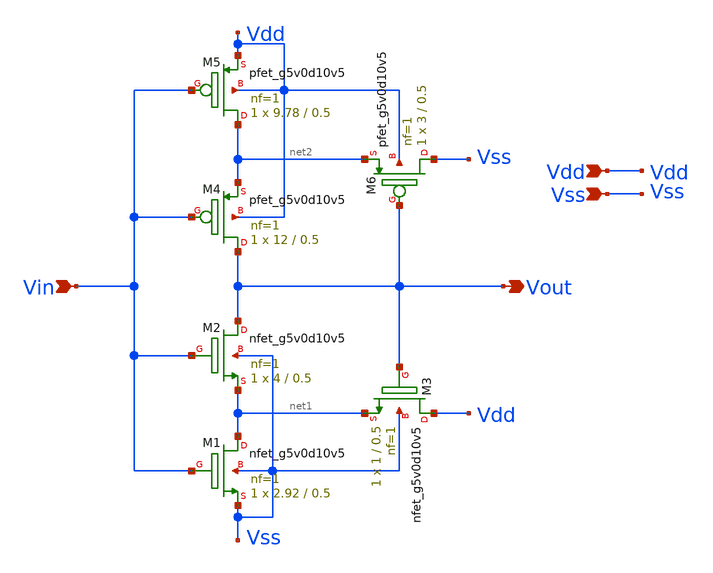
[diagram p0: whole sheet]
** sch_path: xschem/Schmitt.sch
**.subckt Schmitt Vout Vin Vdd Vss
*.opin Vout
*.ipin Vin
*.ipin Vdd
*.ipin Vss
XM1 net1 Vin Vss Vss sky130_fd_pr__nfet_g5v0d10v5 L=0.5 W=2.92 nf=1 ad='int((1 + 1)/2) * 2.92 / 1 * 0.29'
+ as='int((1 + 2)/2) * 2.92 / 1 * 0.29' pd='2*int((1 + 1)/2) * (2.92 / 1 + 0.29)' ps='2*int((1 + 2)/2) * (2.92 / 1 + 0.29)'
+ nrd='0.29 / 2.92 ' nrs='0.29 / 2.92 ' sa=0 sb=0 sd=0 mult=1 m=1
XM5 net2 Vin Vdd Vdd sky130_fd_pr__pfet_g5v0d10v5 L=0.5 W=9.78 nf=1 ad='int((1 + 1)/2) * 9.78 / 1 * 0.29'
+ as='int((1 + 2)/2) * 9.78 / 1 * 0.29' pd='2*int((1 + 1)/2) * (9.78 / 1 + 0.29)' ps='2*int((1 + 2)/2) * (9.78 / 1 + 0.29)'
+ nrd='0.29 / 9.78 ' nrs='0.29 / 9.78 ' sa=0 sb=0 sd=0 mult=1 m=1
XM3 Vdd Vout net1 Vss sky130_fd_pr__nfet_g5v0d10v5 L=0.5 W=1 nf=1 ad='int((1 + 1)/2) * 1 / 1 * 0.29'
+ as='int((1 + 2)/2) * 1 / 1 * 0.29' pd='2*int((1 + 1)/2) * (1 / 1 + 0.29)' ps='2*int((1 + 2)/2) * (1 / 1 + 0.29)'
+ nrd='0.29 / 1 ' nrs='0.29 / 1 ' sa=0 sb=0 sd=0 mult=1 m=1
XM2 Vout Vin net1 Vss sky130_fd_pr__nfet_g5v0d10v5 L=0.5 W=4 nf=1 ad='int((1 + 1)/2) * 4 / 1 * 0.29'
+ as='int((1 + 2)/2) * 4 / 1 * 0.29' pd='2*int((1 + 1)/2) * (4 / 1 + 0.29)' ps='2*int((1 + 2)/2) * (4 / 1 + 0.29)'
+ nrd='0.29 / 4 ' nrs='0.29 / 4 ' sa=0 sb=0 sd=0 mult=1 m=1
XM6 Vss Vout net2 Vdd sky130_fd_pr__pfet_g5v0d10v5 L=0.5 W=3 nf=1 ad='int((1 + 1)/2) * 3 / 1 * 0.29'
+ as='int((1 + 2)/2) * 3 / 1 * 0.29' pd='2*int((1 + 1)/2) * (3 / 1 + 0.29)' ps='2*int((1 + 2)/2) * (3 / 1 + 0.29)'
+ nrd='0.29 / 3 ' nrs='0.29 / 3 ' sa=0 sb=0 sd=0 mult=1 m=1
XM4 Vout Vin net2 Vdd sky130_fd_pr__pfet_g5v0d10v5 L=0.5 W=12 nf=1 ad='int((1 + 1)/2) * 12 / 1 * 0.29'
+ as='int((1 + 2)/2) * 12 / 1 * 0.29' pd='2*int((1 + 1)/2) * (12 / 1 + 0.29)' ps='2*int((1 + 2)/2) * (12 / 1 + 0.29)'
+ nrd='0.29 / 12 ' nrs='0.29 / 12 ' sa=0 sb=0 sd=0 mult=1 m=1
**.ends
.end
